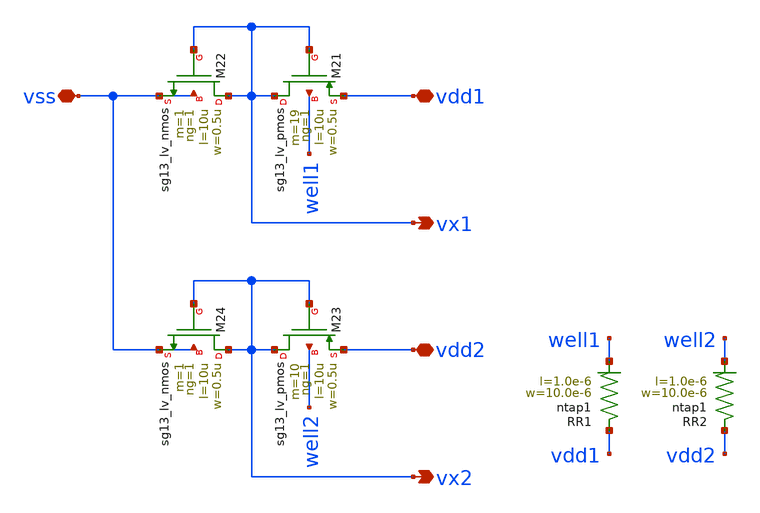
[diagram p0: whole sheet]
** sch_path: Layouts/comp_w_hyst/inverters.sch
**.subckt inverters vss vdd1 vdd2 vx1 vx2
*.iopin vss
*.iopin vdd1
*.iopin vdd2
*.opin vx1
*.opin vx2
XM21 vx1 vx1 vdd1 well1 sg13_lv_pmos w=0.5u l=10u ng=1 m=19 mm_ok=1
XM22 vx1 vx1 vss vss sg13_lv_nmos w=0.5u l=10u ng=1 m=1 mm_ok=1
XM23 vx2 vx2 vdd2 well2 sg13_lv_pmos w=0.5u l=10u ng=1 m=10 mm_ok=1
XM24 vx2 vx2 vss vss sg13_lv_nmos w=0.5u l=10u ng=1 m=1 mm_ok=1
XR1 vdd1 well1 ntap1 R=30.62 w=10.0e-6 l=1.0e-6
XR2 vdd2 well2 ntap1 R=30.62 w=10.0e-6 l=1.0e-6
**.ends
.end
